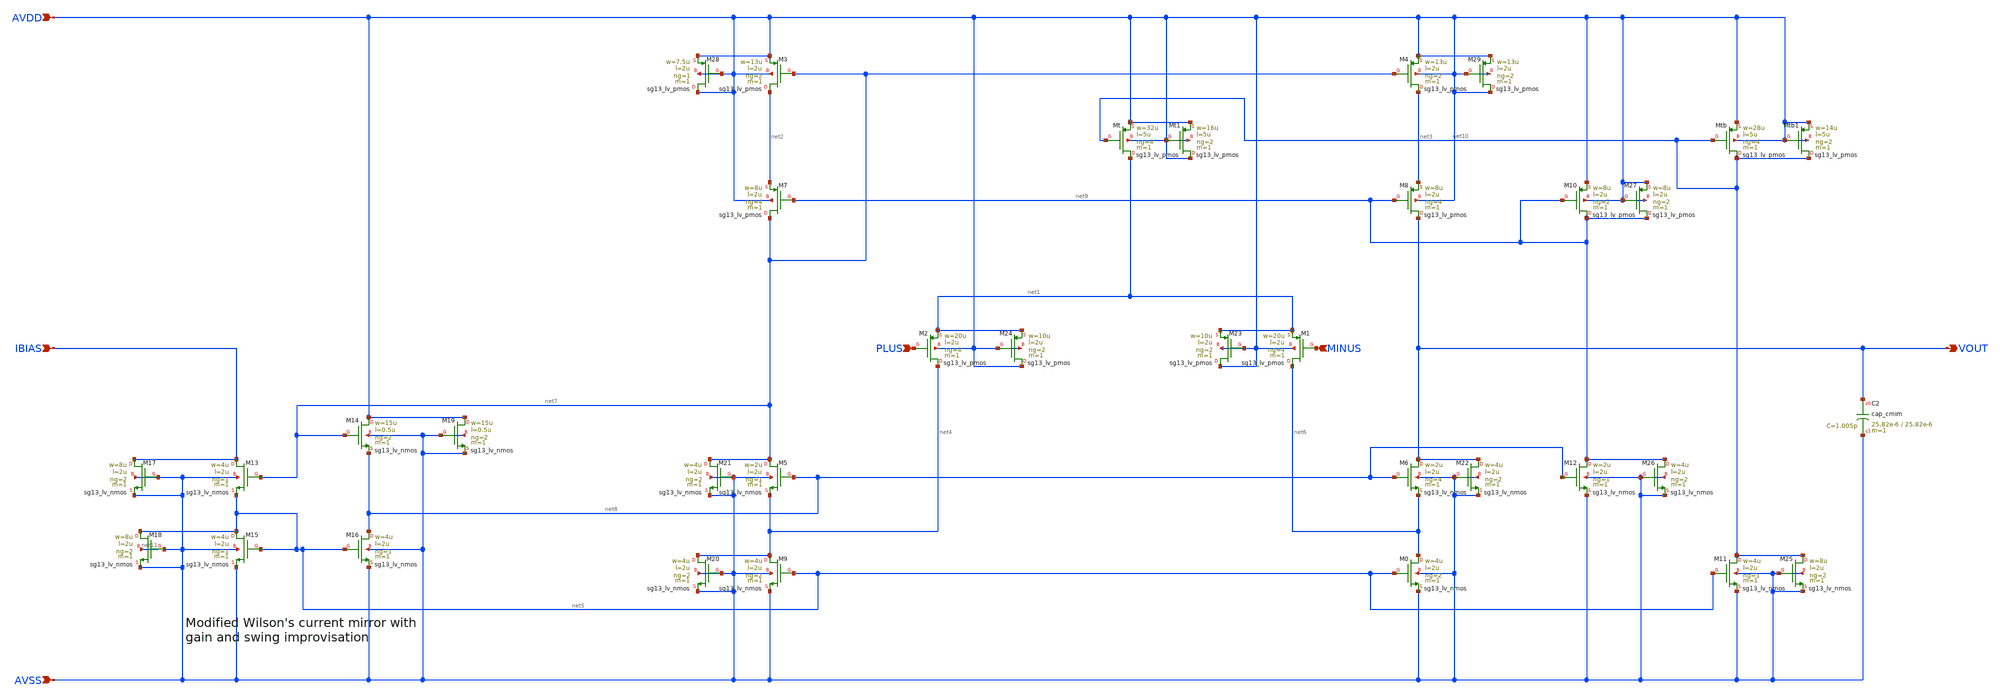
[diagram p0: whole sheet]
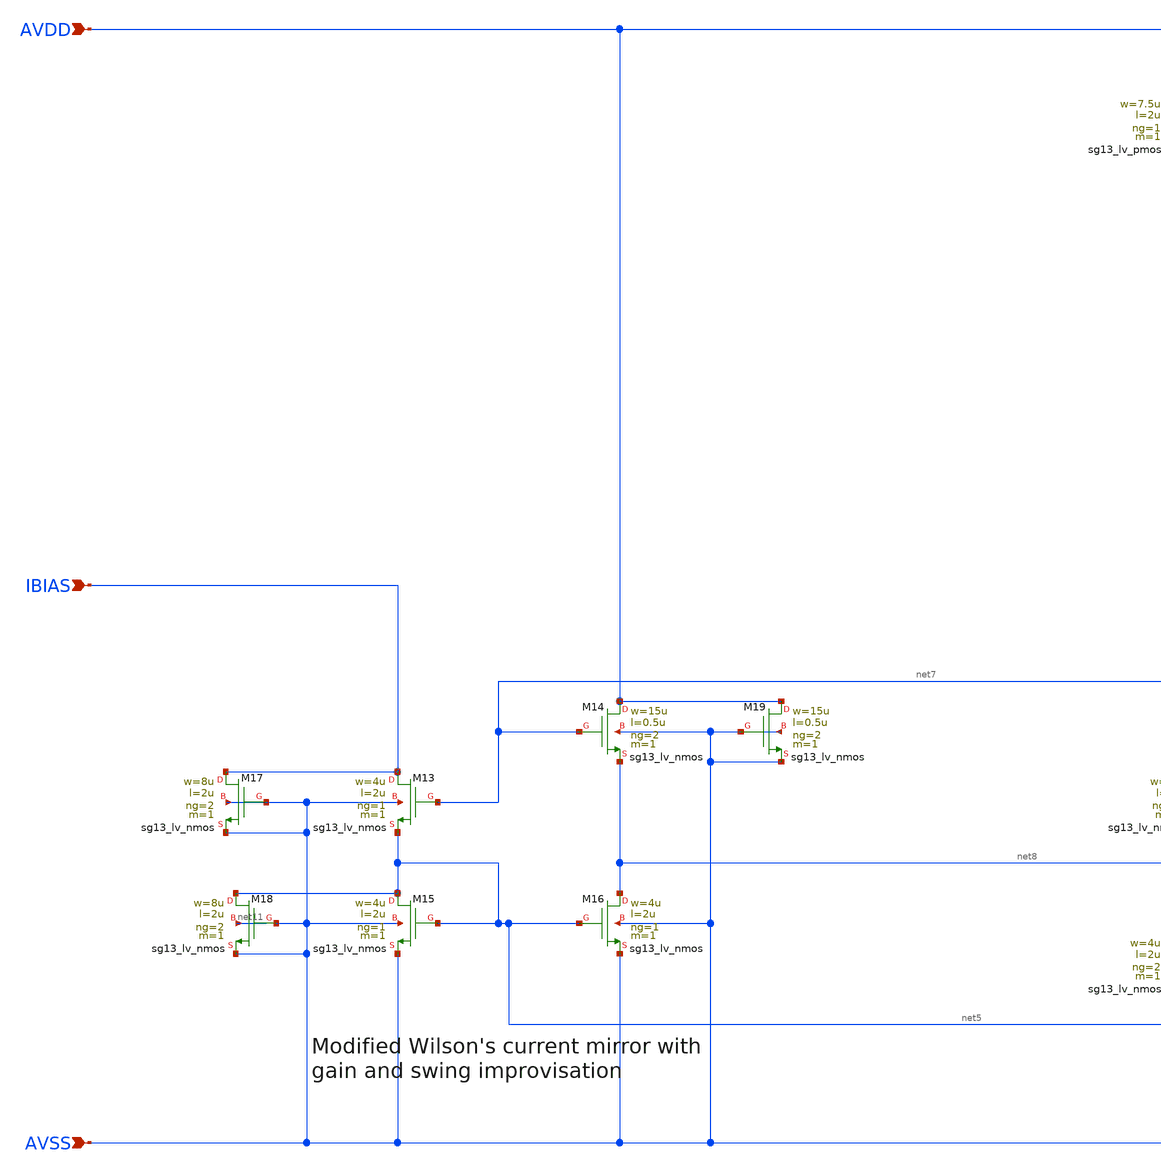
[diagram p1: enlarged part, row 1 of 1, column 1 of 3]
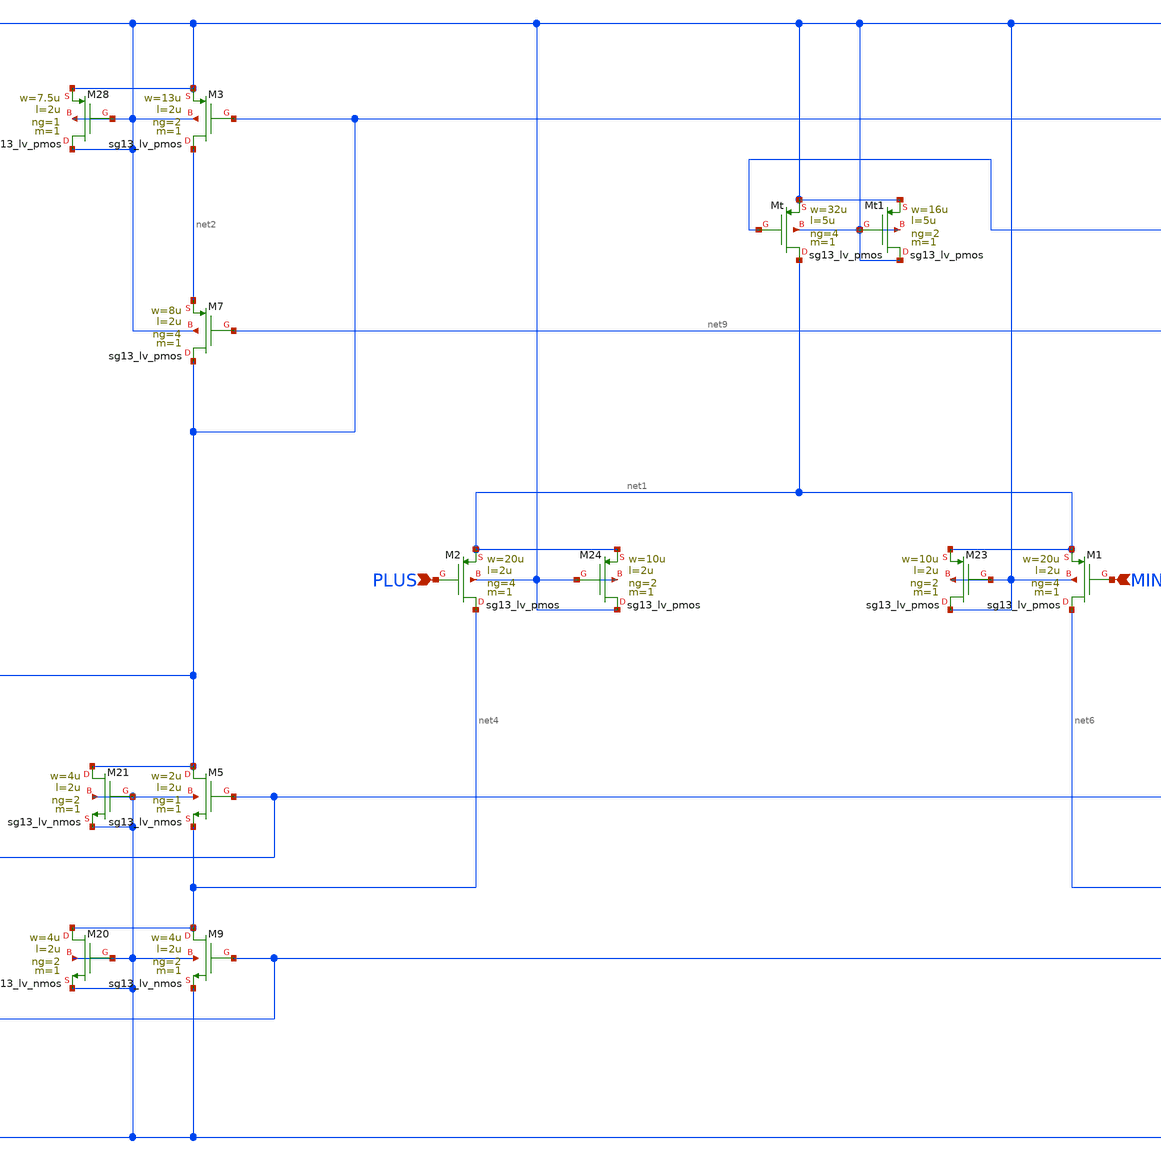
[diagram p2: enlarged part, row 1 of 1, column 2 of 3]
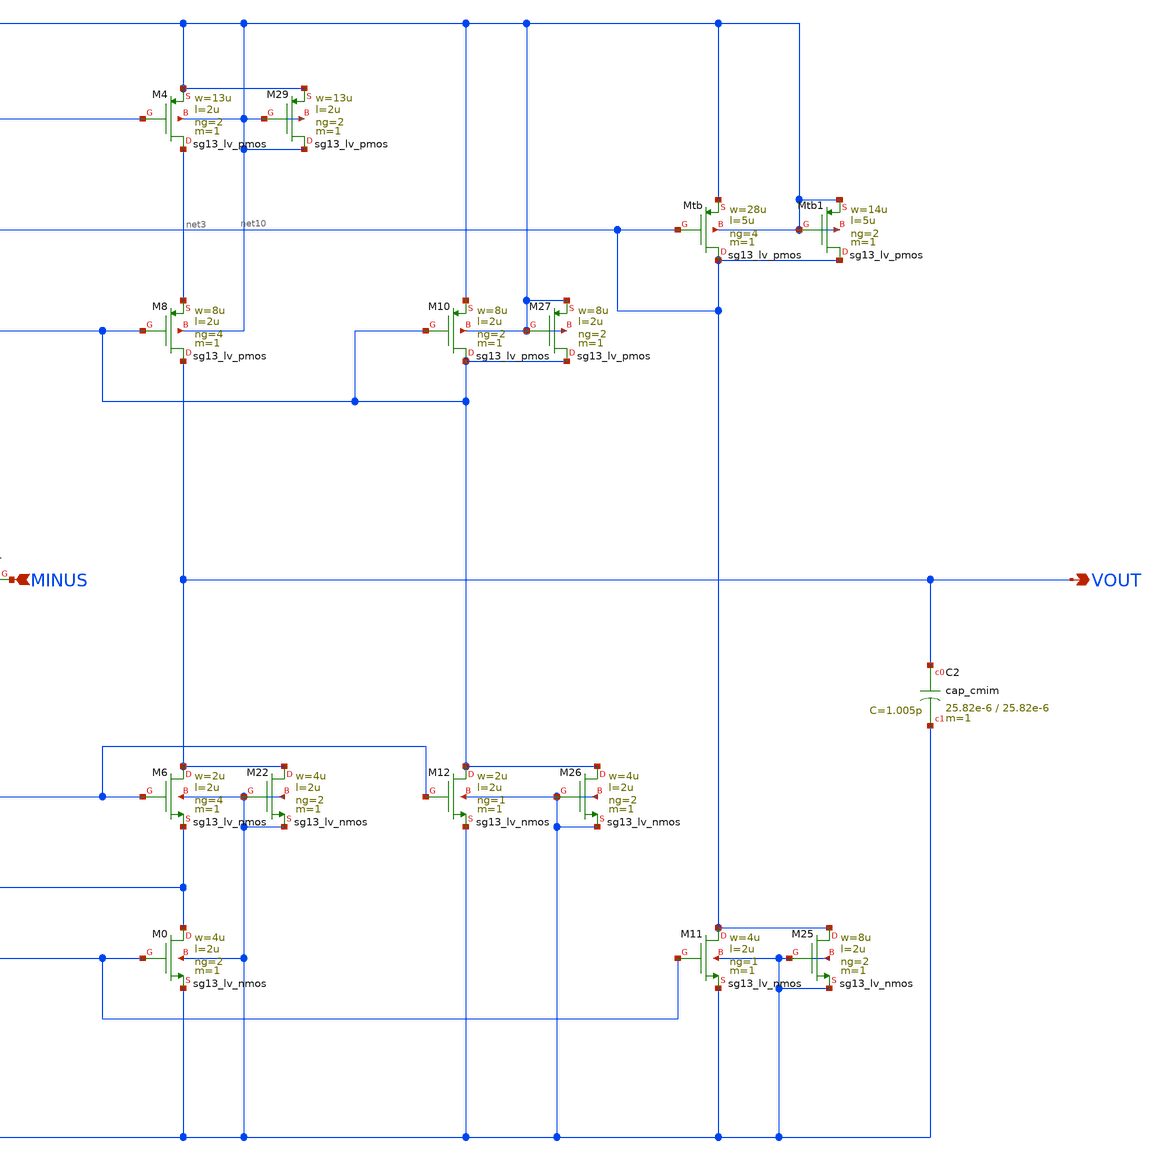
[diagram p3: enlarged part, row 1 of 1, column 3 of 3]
** sch_path: Designs/otas/1_schematics/foldedcascode_pmos.sch
**.subckt foldedcascode_pmos AVDD AVSS IBIAS PLUS MINUS VOUT
*.ipin AVDD
*.ipin AVSS
*.ipin IBIAS
*.ipin PLUS
*.ipin MINUS
*.opin VOUT
XM1 net6 MINUS net1 AVDD sg13_lv_pmos w=20u l=2u ng=4 m=1 mm_ok=1
XM5 net7 net8 net4 AVSS sg13_lv_nmos w=2u l=2u ng=1 m=1 mm_ok=1
XM2 net4 PLUS net1 AVDD sg13_lv_pmos w=20u l=2u ng=4 m=1 mm_ok=1
XM3 net2 net7 AVDD AVDD sg13_lv_pmos w=13u l=2u ng=2 m=1 mm_ok=1
XM4 net3 net7 AVDD AVDD sg13_lv_pmos w=13u l=2u ng=2 m=1 mm_ok=1
XM7 net7 net9 net2 AVDD sg13_lv_pmos w=8u l=2u ng=4 m=1 mm_ok=1
XM8 VOUT net9 net3 AVDD sg13_lv_pmos w=8u l=2u ng=4 m=1 mm_ok=1
XM6 VOUT net8 net6 AVSS sg13_lv_nmos w=2u l=2u ng=4 m=1 mm_ok=1
XM9 net4 net5 AVSS AVSS sg13_lv_nmos w=4u l=2u ng=2 m=1 mm_ok=1
XM0 net6 net5 AVSS AVSS sg13_lv_nmos w=4u l=2u ng=2 m=1 mm_ok=1
XMt net1 net10 AVDD AVDD sg13_lv_pmos w=32u l=5u ng=4 m=1 mm_ok=1
XM13 IBIAS net7 net5 AVSS sg13_lv_nmos w=4u l=2u ng=1 m=1 mm_ok=1
XM15 net5 net5 AVSS AVSS sg13_lv_nmos w=4u l=2u ng=1 m=1 mm_ok=1
XM16 net8 net5 AVSS AVSS sg13_lv_nmos w=4u l=2u ng=1 m=1 mm_ok=1
XM14 AVDD net7 net8 AVSS sg13_lv_nmos w=15u l=0.5u ng=2 m=1 mm_ok=1
XM12 net9 net8 AVSS AVSS sg13_lv_nmos w=2u l=2u ng=1 m=1 mm_ok=1
XM10 net9 net9 AVDD AVDD sg13_lv_pmos w=8u l=2u ng=2 m=1 mm_ok=1
XM11 net10 net5 AVSS AVSS sg13_lv_nmos w=4u l=2u ng=1 m=1 mm_ok=1
XMtb net10 net10 AVDD AVDD sg13_lv_pmos w=28u l=5u ng=4 m=1 mm_ok=1
XC2 VOUT AVSS cap_cmim w=25.82e-6 l=25.82e-6 m=1 mm_ok=1
XM17 IBIAS AVSS AVSS AVSS sg13_lv_nmos w=8u l=2u ng=2 m=1 mm_ok=1
XM18 net5 AVSS AVSS net11 sg13_lv_nmos w=8u l=2u ng=2 m=1 mm_ok=1
XM19 AVDD AVSS AVSS AVSS sg13_lv_nmos w=15u l=0.5u ng=2 m=1 mm_ok=1
XM20 net4 AVSS AVSS AVSS sg13_lv_nmos w=4u l=2u ng=2 m=1 mm_ok=1
XM21 net7 AVSS AVSS AVSS sg13_lv_nmos w=4u l=2u ng=2 m=1 mm_ok=1
XM22 VOUT AVSS AVSS AVSS sg13_lv_nmos w=4u l=2u ng=2 m=1 mm_ok=1
XM23 AVDD AVDD net1 AVDD sg13_lv_pmos w=10u l=2u ng=2 m=1 mm_ok=1
XM24 AVDD AVDD net1 AVDD sg13_lv_pmos w=10u l=2u ng=2 m=1 mm_ok=1
XM25 net10 AVSS AVSS AVSS sg13_lv_nmos w=8u l=2u ng=2 m=1 mm_ok=1
XM26 net9 AVSS AVSS AVSS sg13_lv_nmos w=4u l=2u ng=2 m=1 mm_ok=1
XMtb1 net10 AVDD AVDD AVDD sg13_lv_pmos w=14u l=5u ng=2 m=1 mm_ok=1
XM27 net9 AVDD AVDD AVDD sg13_lv_pmos w=8u l=2u ng=2 m=1 mm_ok=1
XMt1 AVDD AVDD AVDD AVDD sg13_lv_pmos w=16u l=5u ng=2 m=1 mm_ok=1
XM28 AVDD AVDD AVDD AVDD sg13_lv_pmos w=7.5u l=2u ng=1 m=1 mm_ok=1
XM29 AVDD AVDD AVDD AVDD sg13_lv_pmos w=13u l=2u ng=2 m=1 mm_ok=1
**.ends
.end
